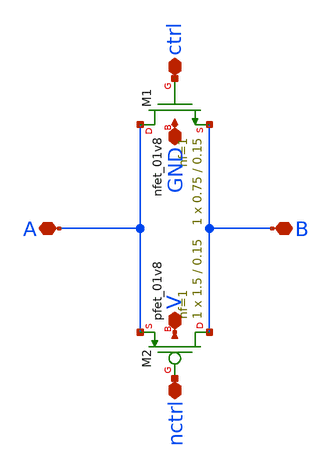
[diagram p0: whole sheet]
** sch_path: xschem/designs/counter4b/tgate.sch
**.subckt tgate ctrl A B nctrl GND V
*.iopin ctrl
*.iopin A
*.iopin B
*.iopin nctrl
*.iopin GND
*.iopin V
XM1 A ctrl B GND sky130_fd_pr__nfet_01v8 L=0.15 W=0.75 nf=1 ad='int((nf+1)/2) * W/nf * 0.29' as='int((nf+2)/2) * W/nf * 0.29'
+ pd='2*int((nf+1)/2) * (W/nf + 0.29)' ps='2*int((nf+2)/2) * (W/nf + 0.29)' nrd='0.29 / W' nrs='0.29 / W'
+ sa=0 sb=0 sd=0 mult=1 m=1
XM2 B nctrl A V sky130_fd_pr__pfet_01v8 L=0.15 W=1.5 nf=1 ad='int((nf+1)/2) * W/nf * 0.29' as='int((nf+2)/2) * W/nf * 0.29'
+ pd='2*int((nf+1)/2) * (W/nf + 0.29)' ps='2*int((nf+2)/2) * (W/nf + 0.29)' nrd='0.29 / W' nrs='0.29 / W'
+ sa=0 sb=0 sd=0 mult=1 m=1
**.ends
.end
